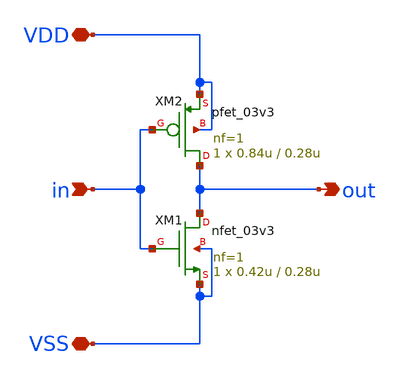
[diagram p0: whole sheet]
** sch_path: adc_sar_inverter.sch
**.subckt adc_sar_inverter VDD VSS in out
*.iopin VDD
*.iopin VSS
*.ipin in
*.opin out
XM1 out in VSS VSS nfet_03v3 L=0.28u W=0.42u nf=1 ad='int((nf+1)/2) * W/nf * 0.18u' as='int((nf+2)/2) * W/nf * 0.18u'
+ pd='2*int((nf+1)/2) * (W/nf + 0.18u)' ps='2*int((nf+2)/2) * (W/nf + 0.18u)' nrd='0.18u / W' nrs='0.18u / W'
+ sa=0 sb=0 sd=0 m=1
XM2 out in VDD VDD pfet_03v3 L=0.28u W=0.84u nf=1 ad='int((nf+1)/2) * W/nf * 0.18u' as='int((nf+2)/2) * W/nf * 0.18u'
+ pd='2*int((nf+1)/2) * (W/nf + 0.18u)' ps='2*int((nf+2)/2) * (W/nf + 0.18u)' nrd='0.18u / W' nrs='0.18u / W'
+ sa=0 sb=0 sd=0 m=1
**.ends
.end
